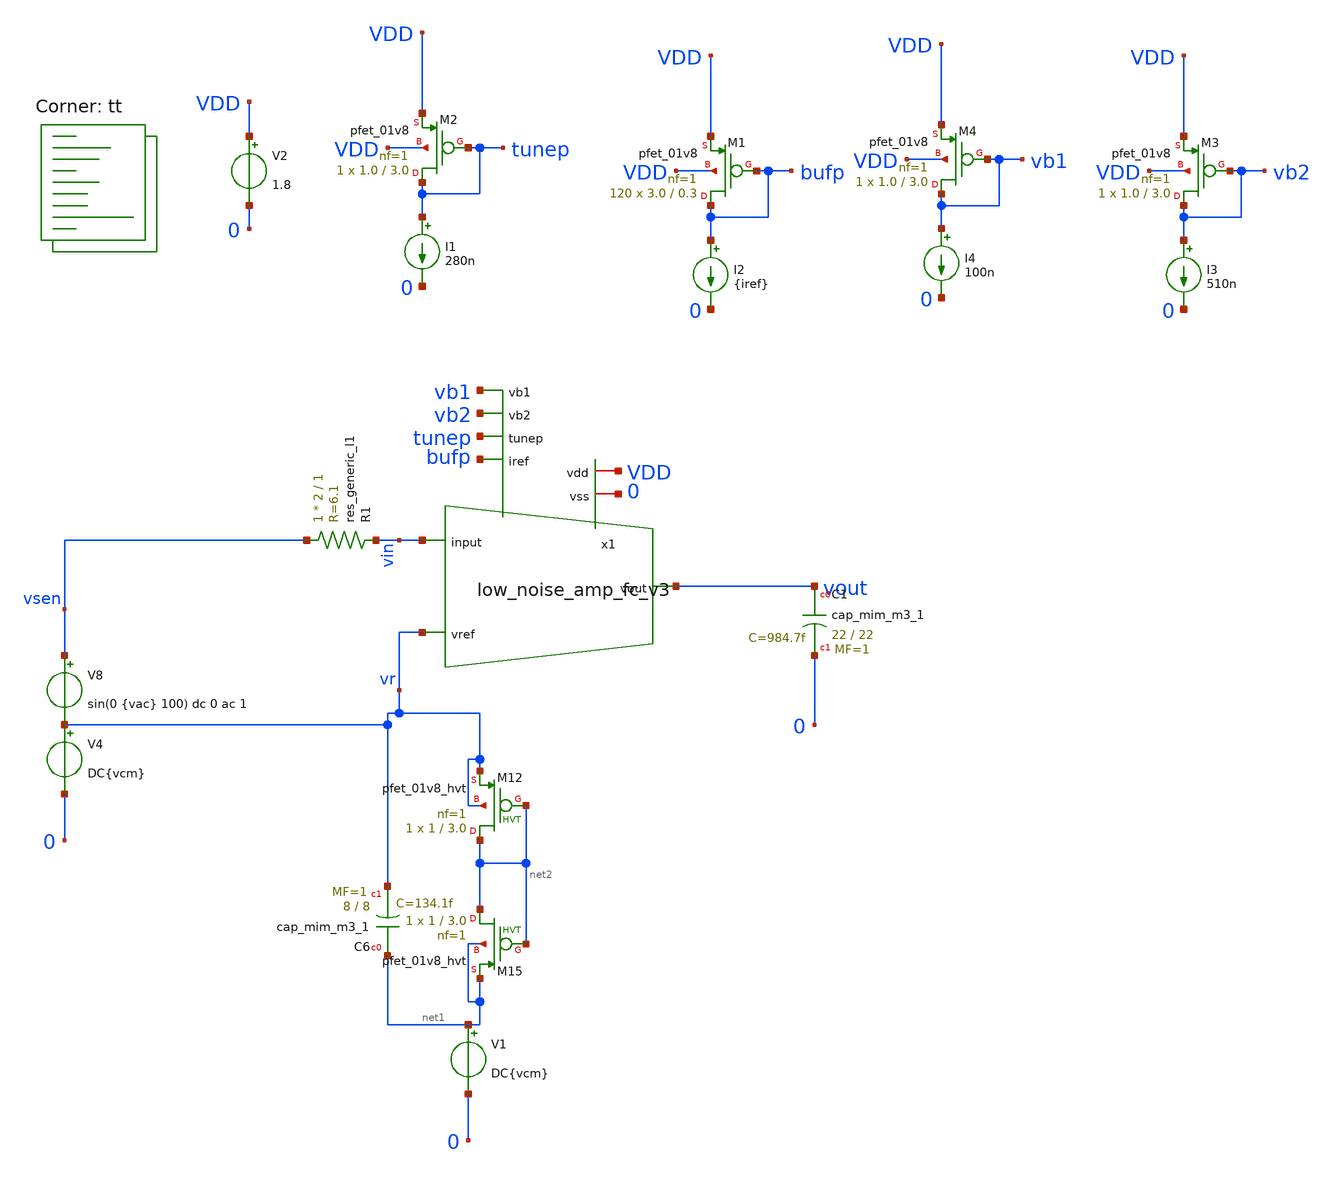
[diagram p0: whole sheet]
** sch_path: design/xschem/low_noise_amp_fc_v3_loopgain_tb.sch
**.subckt low_noise_amp_fc_v3_loopgain_tb
V2 VDD 0 1.8
XC1 vout 0 sky130_fd_pr__cap_mim_m3_1 W=22 L=22 MF=1 m=1
XM1 bufp bufp VDD VDD sky130_fd_pr__pfet_01v8 L=0.3 W=3.0 nf=1 ad='W * 0.29' as='W * 0.29' pd='2 * (W + 0.29)'
+ ps='2 * (W + 0.29)' nrd='0.29 / W' nrs='0.29 / W' sa=0 sb=0 sd=0 mult=120 m=120
I2 bufp 0 {iref}
V8 vsen vr sin(0 {vac} 100) dc 0 ac 1
R1 vsen vin sky130_fd_pr__res_generic_l1 W=2 L=1 m=1
XM2 tunep tunep VDD VDD sky130_fd_pr__pfet_01v8 L=3.0 W=1.0 nf=1 ad='W * 0.29' as='W * 0.29' pd='2 * (W + 0.29)'
+ ps='2 * (W + 0.29)' nrd='0.29 / W' nrs='0.29 / W' sa=0 sb=0 sd=0 mult=1 m=1
I1 tunep 0 280n
x1 0 vb1 vb2 vout vin VDD bufp vr tunep low_noise_amp_fc_v3
I3 vb2 0 510n
XM4 vb1 vb1 VDD VDD sky130_fd_pr__pfet_01v8 L=3.0 W=1.0 nf=1 ad='W * 0.29' as='W * 0.29' pd='2 * (W + 0.29)'
+ ps='2 * (W + 0.29)' nrd='0.29 / W' nrs='0.29 / W' sa=0 sb=0 sd=0 mult=1 m=1
I4 vb1 0 100n
XM3 vb2 vb2 VDD VDD sky130_fd_pr__pfet_01v8 L=3.0 W=1.0 nf=1 ad='W * 0.29' as='W * 0.29' pd='2 * (W + 0.29)'
+ ps='2 * (W + 0.29)' nrd='0.29 / W' nrs='0.29 / W' sa=0 sb=0 sd=0 mult=1 m=1
V1 net1 0 DC{vcm}
XC6 net1 vr sky130_fd_pr__cap_mim_m3_1 W=8 L=8 MF=1 m=1
XM12 net2 net2 vr vr sky130_fd_pr__pfet_01v8_hvt L=3.0 W=1 nf=1 ad='int((nf+1)/2) * W/nf * 0.29' as='int((nf+2)/2) * W/nf * 0.29'
+ pd='2*int((nf+1)/2) * (W/nf + 0.29)' ps='2*int((nf+2)/2) * (W/nf + 0.29)' nrd='0.29 / W' nrs='0.29 / W'
+ sa=0 sb=0 sd=0 mult=1 m=1
XM15 net2 net2 net1 net1 sky130_fd_pr__pfet_01v8_hvt L=3.0 W=1 nf=1 ad='int((nf+1)/2) * W/nf * 0.29'
+ as='int((nf+2)/2) * W/nf * 0.29' pd='2*int((nf+1)/2) * (W/nf + 0.29)' ps='2*int((nf+2)/2) * (W/nf + 0.29)'
+ nrd='0.29 / W' nrs='0.29 / W' sa=0 sb=0 sd=0 mult=1 m=1
V4 vr 0 DC{vcm}
**** begin user architecture code
.lib $::SKYWATER_MODELS/sky130.lib.spice tt



* ngspice commands



* Circuit Parameters
*.param iref1 = 200u
.param iref = 6u
.param vdd  = 1.8
.param vss  = 0.0
.param vcm  = 0.8
.param vac  = 5u
.options TEMP = 35.0


* OP Parameters & Singals to save
.save all

  @M.X1.XM2.msky130_fd_pr__pfet_01v8[id] @M.X1.XM2.msky130_fd_pr__pfet_01v8[vth]
+ @M.X1.XM2.msky130_fd_pr__pfet_01v8[vgs] @M.X1.XM2.msky130_fd_pr__pfet_01v8[vds] @M.X1.XM2.msky130_fd_pr__pfet_01v8[vdsat]
+ @M.X1.XM2.msky130_fd_pr__pfet_01v8[gm] @M.X1.XM2.msky130_fd_pr__pfet_01v8[gds] @M.X1.XM2.msky130_fd_pr__pfet_01v8[cgs]
+  @M.X1.XM1.msky130_fd_pr__pfet_01v8[id] @M.X1.XM1.msky130_fd_pr__pfet_01v8[vth] @M.X1.XM1.msky130_fd_pr__pfet_01v8[vgs]
+ @M.X1.XM1.msky130_fd_pr__pfet_01v8[vds] @M.X1.XM1.msky130_fd_pr__pfet_01v8[vdsat] @M.X1.XM1.msky130_fd_pr__pfet_01v8[gm]
+ @M.X1.XM1.msky130_fd_pr__pfet_01v8[gds]  @M.X1.XM5.msky130_fd_pr__pfet_01v8[id] @M.X1.XM5.msky130_fd_pr__pfet_01v8[vth]
+ @M.X1.XM5.msky130_fd_pr__pfet_01v8[vgs] @M.X1.XM5.msky130_fd_pr__pfet_01v8[vds] @M.X1.XM5.msky130_fd_pr__pfet_01v8[vdsat]
+ @M.X1.XM5.msky130_fd_pr__pfet_01v8[gm] @M.X1.XM5.msky130_fd_pr__pfet_01v8[gds]

  @M.X1.XM3.msky130_fd_pr__nfet_01v8[id] @M.X1.XM3.msky130_fd_pr__nfet_01v8[vth]
+ @M.X1.XM3.msky130_fd_pr__nfet_01v8[vgs] @M.X1.XM3.msky130_fd_pr__nfet_01v8[vds] @M.X1.XM3.msky130_fd_pr__nfet_01v8[vdsat]
+ @M.X1.XM3.msky130_fd_pr__nfet_01v8[gm] @M.X1.XM3.msky130_fd_pr__nfet_01v8[gds]  @M.X1.XM6.msky130_fd_pr__nfet_01v8[id]
+ @M.X1.XM6.msky130_fd_pr__nfet_01v8[vth] @M.X1.XM6.msky130_fd_pr__nfet_01v8[vgs] @M.X1.XM6.msky130_fd_pr__nfet_01v8[vds]
+ @M.X1.XM6.msky130_fd_pr__nfet_01v8[vdsat] @M.X1.XM6.msky130_fd_pr__nfet_01v8[gm] @M.X1.XM6.msky130_fd_pr__nfet_01v8[gds]
+  @M.X1.XM4.msky130_fd_pr__nfet_01v8[id] @M.X1.XM4.msky130_fd_pr__nfet_01v8[vth] @M.X1.XM4.msky130_fd_pr__nfet_01v8[vgs]
+ @M.X1.XM4.msky130_fd_pr__nfet_01v8[vds] @M.X1.XM4.msky130_fd_pr__nfet_01v8[vdsat] @M.X1.XM4.msky130_fd_pr__nfet_01v8[gm]
+ @M.X1.XM4.msky130_fd_pr__nfet_01v8[gds]  @M.X1.XM9.msky130_fd_pr__nfet_01v8[id] @M.X1.XM9.msky130_fd_pr__nfet_01v8[vth]
+ @M.X1.XM9.msky130_fd_pr__nfet_01v8[vgs] @M.X1.XM9.msky130_fd_pr__nfet_01v8[vds] @M.X1.XM9.msky130_fd_pr__nfet_01v8[vdsat]
+ @M.X1.XM9.msky130_fd_pr__nfet_01v8[gm] @M.X1.XM9.msky130_fd_pr__nfet_01v8[gds]
  @M.X1.XM10.msky130_fd_pr__nfet_01v8[id] @M.X1.XM10.msky130_fd_pr__nfet_01v8[vth]
+ @M.X1.XM10.msky130_fd_pr__nfet_01v8[vgs] @M.X1.XM10.msky130_fd_pr__nfet_01v8[vds] @M.X1.XM10.msky130_fd_pr__nfet_01v8[vdsat]
+ @M.X1.XM10.msky130_fd_pr__nfet_01v8[gm] @M.X1.XM10.msky130_fd_pr__nfet_01v8[gds]  @M.X1.XM15.msky130_fd_pr__nfet_01v8[id]
+ @M.X1.XM15.msky130_fd_pr__nfet_01v8[vth] @M.X1.XM15.msky130_fd_pr__nfet_01v8[vgs] @M.X1.XM15.msky130_fd_pr__nfet_01v8[vds]
+ @M.X1.XM15.msky130_fd_pr__nfet_01v8[vdsat] @M.X1.XM15.msky130_fd_pr__nfet_01v8[gm] @M.X1.XM15.msky130_fd_pr__nfet_01v8[gds]
+  @M.X1.XM12.msky130_fd_pr__nfet_01v8[id] @M.X1.XM12.msky130_fd_pr__nfet_01v8[vth] @M.X1.XM12.msky130_fd_pr__nfet_01v8[vgs]
+ @M.X1.XM12.msky130_fd_pr__nfet_01v8[vds] @M.X1.XM12.msky130_fd_pr__nfet_01v8[vdsat] @M.X1.XM12.msky130_fd_pr__nfet_01v8[gm]
+ @M.X1.XM12.msky130_fd_pr__nfet_01v8[gds]  @M.X1.XM7.msky130_fd_pr__nfet_01v8[id] @M.X1.XM7.msky130_fd_pr__nfet_01v8[vth]
+ @M.X1.XM7.msky130_fd_pr__nfet_01v8[vgs] @M.X1.XM7.msky130_fd_pr__nfet_01v8[vds] @M.X1.XM7.msky130_fd_pr__nfet_01v8[vdsat]
+ @M.X1.XM7.msky130_fd_pr__nfet_01v8[gm] @M.X1.XM7.msky130_fd_pr__nfet_01v8[gds]
  @M.X1.XM16.msky130_fd_pr__pfet_01v8[id] @M.X1.XM16.msky130_fd_pr__pfet_01v8[vth]
+ @M.X1.XM16.msky130_fd_pr__pfet_01v8[vgs] @M.X1.XM16.msky130_fd_pr__pfet_01v8[vds] @M.X1.XM16.msky130_fd_pr__pfet_01v8[vdsat]
+ @M.X1.XM16.msky130_fd_pr__pfet_01v8[gm] @M.X1.XM16.msky130_fd_pr__pfet_01v8[gds]  @M.X1.XM27.msky130_fd_pr__pfet_01v8[id]
+ @M.X1.XM27.msky130_fd_pr__pfet_01v8[vth] @M.X1.XM27.msky130_fd_pr__pfet_01v8[vgs] @M.X1.XM27.msky130_fd_pr__pfet_01v8[vds]
+ @M.X1.XM27.msky130_fd_pr__pfet_01v8[vdsat] @M.X1.XM27.msky130_fd_pr__pfet_01v8[gm] @M.X1.XM27.msky130_fd_pr__pfet_01v8[gds]
+  @M.X1.XM17.msky130_fd_pr__pfet_01v8[id] @M.X1.XM17.msky130_fd_pr__pfet_01v8[vth] @M.X1.XM17.msky130_fd_pr__pfet_01v8[vgs]
+ @M.X1.XM17.msky130_fd_pr__pfet_01v8[vds] @M.X1.XM17.msky130_fd_pr__pfet_01v8[vdsat] @M.X1.XM17.msky130_fd_pr__pfet_01v8[gm]
+ @M.X1.XM17.msky130_fd_pr__pfet_01v8[gds]  @M.X1.XM24.msky130_fd_pr__pfet_01v8[id] @M.X1.XM24.msky130_fd_pr__pfet_01v8[vth]
+ @M.X1.XM24.msky130_fd_pr__pfet_01v8[vgs] @M.X1.XM24.msky130_fd_pr__pfet_01v8[vds] @M.X1.XM24.msky130_fd_pr__pfet_01v8[vdsat]
+ @M.X1.XM24.msky130_fd_pr__pfet_01v8[gm] @M.X1.XM24.msky130_fd_pr__pfet_01v8[gds]  @M.X1.XM25.msky130_fd_pr__pfet_01v8[id]
+ @M.X1.XM25.msky130_fd_pr__pfet_01v8[vth] @M.X1.XM25.msky130_fd_pr__pfet_01v8[vgs] @M.X1.XM25.msky130_fd_pr__pfet_01v8[vds]
+ @M.X1.XM25.msky130_fd_pr__pfet_01v8[vdsat] @M.X1.XM25.msky130_fd_pr__pfet_01v8[gm] @M.X1.XM25.msky130_fd_pr__pfet_01v8[gds]
+  @M.X1.XM26.msky130_fd_pr__pfet_01v8[id] @M.X1.XM26.msky130_fd_pr__pfet_01v8[vth] @M.X1.XM26.msky130_fd_pr__pfet_01v8[vgs]
+ @M.X1.XM26.msky130_fd_pr__pfet_01v8[vds] @M.X1.XM26.msky130_fd_pr__pfet_01v8[vdsat] @M.X1.XM26.msky130_fd_pr__pfet_01v8[gm]
+ @M.X1.XM26.msky130_fd_pr__pfet_01v8[gds]



*Simulations
.control
  ac dec 200 0.001 1G
  setplot ac1
  meas ac GBW when vdb(vout)=0
  meas ac DCG find vdb(vout) at=10
  meas ac PM find vp(vout) when vdb(vout)=0
  print PM*180/PI
  meas ac GM find vdb(vout) when vp(vout)=0
  plot vdb(vout) {vp(vout)*180/PI}
  write opamp_closeloop_ac1_v1.raw

  reset
  tran 1u 120m
  setplot tran1
  plot v(vsen) v(vout)
  write opamp_closeloop_tran1.raw

  reset
  noise v(vout) V8 dec 200 0.001 1G 1
  setplot noise1
  plot inoise_spectrum onoise_spectrum
  *print inoise_spectrum
  *print onoise_spectrum
  setplot noise2
  *plot inoise_total onoise_total
  print inoise_total
  print onoise_total
  print frequency inoise_spectrum onoise_spectrum > noise_data.csv
  write opamp_closeloop_noise_v1.raw

  reset
  op
  setplot op1
  print vout
  write opamp_closeloop_op1_v3_fctoday.raw

.endc

.end



**** end user architecture code
**.ends

* expanding   symbol:  low_noise_amp_fc_v3.sym # of pins=10
** sym_path: design/xschem/low_noise_amp_fc_v3.sym
** sch_path: design/xschem/low_noise_amp_fc_v3.sch
.subckt low_noise_amp_fc_v3 vss vb1 vb2 vout input vdd iref vref tunep
*.iopin vdd
*.iopin vss
*.ipin vref
*.ipin iref
*.ipin input
*.opin vout
*.ipin tunep
*.ipin vb1
*.ipin vb2
XM1 vy vin vp vdd sky130_fd_pr__pfet_01v8 L=2.0 W=4.0 nf=1 ad='W * 0.29' as='W * 0.29' pd='2 * (W + 0.29)'
+ ps='2 * (W + 0.29)' nrd='0.29 / W' nrs='0.29 / W' sa=0 sb=0 sd=0 mult=300 m=300
XM2 vx vref vp vdd sky130_fd_pr__pfet_01v8 L=2.0 W=4.0 nf=1 ad='W * 0.29' as='W * 0.29' pd='2 * (W + 0.29)'
+ ps='2 * (W + 0.29)' nrd='0.29 / W' nrs='0.29 / W' sa=0 sb=0 sd=0 mult=300 m=300
XM5 vp iref vdd vdd sky130_fd_pr__pfet_01v8 L=0.3 W=3 nf=1 ad='W * 0.29' as='W * 0.29' pd='2 * (W + 0.29)'
+ ps='2 * (W + 0.29)' nrd='0.29 / W' nrs='0.29 / W' sa=0 sb=0 sd=0 mult=120 m=120
XC6 vin vout sky130_fd_pr__cap_mim_m3_1 W=5 L=5 MF=1 m=1
XM6 vx net1 net2 vss sky130_fd_pr__nfet_01v8 L=20.0 W=8.0 nf=1 ad='W * 0.29' as='W * 0.29' pd='2 * (W + 0.29)'
+ ps='2 * (W + 0.29)' nrd='0.29 / W' nrs='0.29 / W' sa=0 sb=0 sd=0 mult=1 m=1
XM9 vy net1 net3 vss sky130_fd_pr__nfet_01v8 L=20.0 W=8.0 nf=1 ad='W * 0.29' as='W * 0.29' pd='2 * (W + 0.29)'
+ ps='2 * (W + 0.29)' nrd='0.29 / W' nrs='0.29 / W' sa=0 sb=0 sd=0 mult=1 m=1
XM10 net1 net4 vx vss sky130_fd_pr__nfet_01v8 L=1.0 W=10.0 nf=1 ad='W * 0.29' as='W * 0.29' pd='2 * (W + 0.29)'
+ ps='2 * (W + 0.29)' nrd='0.29 / W' nrs='0.29 / W' sa=0 sb=0 sd=0 mult=1 m=1
XM12 vout net7 vy vss sky130_fd_pr__nfet_01v8 L=1.0 W=10.0 nf=1 ad='W * 0.29' as='W * 0.29' pd='2 * (W + 0.29)'
+ ps='2 * (W + 0.29)' nrd='0.29 / W' nrs='0.29 / W' sa=0 sb=0 sd=0 mult=1 m=1
XM15 net4 vx vss vss sky130_fd_pr__nfet_01v8 L=2.0 W=15.0 nf=1 ad='W * 0.29' as='W * 0.29' pd='2 * (W + 0.29)'
+ ps='2 * (W + 0.29)' nrd='0.29 / W' nrs='0.29 / W' sa=0 sb=0 sd=0 mult=1 m=1
XM16 net4 tunep vdd vdd sky130_fd_pr__pfet_01v8 L=3.0 W=1.0 nf=1 ad='W * 0.29' as='W * 0.29' pd='2 * (W + 0.29)'
+ ps='2 * (W + 0.29)' nrd='0.29 / W' nrs='0.29 / W' sa=0 sb=0 sd=0 mult=1 m=1
XM17 net1 vb2 net5 vdd sky130_fd_pr__pfet_01v8 L=3.0 W=1.0 nf=1 ad='W * 0.29' as='W * 0.29' pd='2 * (W + 0.29)'
+ ps='2 * (W + 0.29)' nrd='0.29 / W' nrs='0.29 / W' sa=0 sb=0 sd=0 mult=1 m=1
XM24 vout vb2 net6 vdd sky130_fd_pr__pfet_01v8 L=3.0 W=1.0 nf=1 ad='W * 0.29' as='W * 0.29' pd='2 * (W + 0.29)'
+ ps='2 * (W + 0.29)' nrd='0.29 / W' nrs='0.29 / W' sa=0 sb=0 sd=0 mult=1 m=1
XM25 net5 vb1 vdd vdd sky130_fd_pr__pfet_01v8 L=3.0 W=1.0 nf=1 ad='W * 0.29' as='W * 0.29' pd='2 * (W + 0.29)'
+ ps='2 * (W + 0.29)' nrd='0.29 / W' nrs='0.29 / W' sa=0 sb=0 sd=0 mult=1 m=1
XM26 net6 vb1 vdd vdd sky130_fd_pr__pfet_01v8 L=3.0 W=1.0 nf=1 ad='W * 0.29' as='W * 0.29' pd='2 * (W + 0.29)'
+ ps='2 * (W + 0.29)' nrd='0.29 / W' nrs='0.29 / W' sa=0 sb=0 sd=0 mult=1 m=1
XM7 net7 vy vss vss sky130_fd_pr__nfet_01v8 L=2.0 W=15.0 nf=1 ad='W * 0.29' as='W * 0.29' pd='2 * (W + 0.29)'
+ ps='2 * (W + 0.29)' nrd='0.29 / W' nrs='0.29 / W' sa=0 sb=0 sd=0 mult=1 m=1
XM27 net7 tunep vdd vdd sky130_fd_pr__pfet_01v8 L=3.0 W=1.0 nf=1 ad='W * 0.29' as='W * 0.29' pd='2 * (W + 0.29)'
+ ps='2 * (W + 0.29)' nrd='0.29 / W' nrs='0.29 / W' sa=0 sb=0 sd=0 mult=1.0 m=1.0
XM36 vres vres vin vin sky130_fd_pr__pfet_01v8_hvt L=3.0 W=1.0 nf=1 ad='int((nf+1)/2) * W/nf * 0.29'
+ as='int((nf+2)/2) * W/nf * 0.29' pd='2*int((nf+1)/2) * (W/nf + 0.29)' ps='2*int((nf+2)/2) * (W/nf + 0.29)'
+ nrd='0.29 / W' nrs='0.29 / W' sa=0 sb=0 sd=0 mult=1 m=1
XM37 vres vres vout vout sky130_fd_pr__pfet_01v8_hvt L=3.0 W=1.0 nf=1 ad='int((nf+1)/2) * W/nf * 0.29'
+ as='int((nf+2)/2) * W/nf * 0.29' pd='2*int((nf+1)/2) * (W/nf + 0.29)' ps='2*int((nf+2)/2) * (W/nf + 0.29)'
+ nrd='0.29 / W' nrs='0.29 / W' sa=0 sb=0 sd=0 mult=1 m=1
XM3 net2 net1 vss vss sky130_fd_pr__nfet_01v8 L=20.0 W=8.0 nf=1 ad='W * 0.29' as='W * 0.29' pd='2 * (W + 0.29)'
+ ps='2 * (W + 0.29)' nrd='0.29 / W' nrs='0.29 / W' sa=0 sb=0 sd=0 mult=1 m=1
XM4 net3 net1 vss vss sky130_fd_pr__nfet_01v8 L=20.0 W=8.0 nf=1 ad='W * 0.29' as='W * 0.29' pd='2 * (W + 0.29)'
+ ps='2 * (W + 0.29)' nrd='0.29 / W' nrs='0.29 / W' sa=0 sb=0 sd=0 mult=1 m=1
XC1 vin input sky130_fd_pr__cap_mim_m3_1 W=132 L=70 MF=1 m=1
.ends

.end
